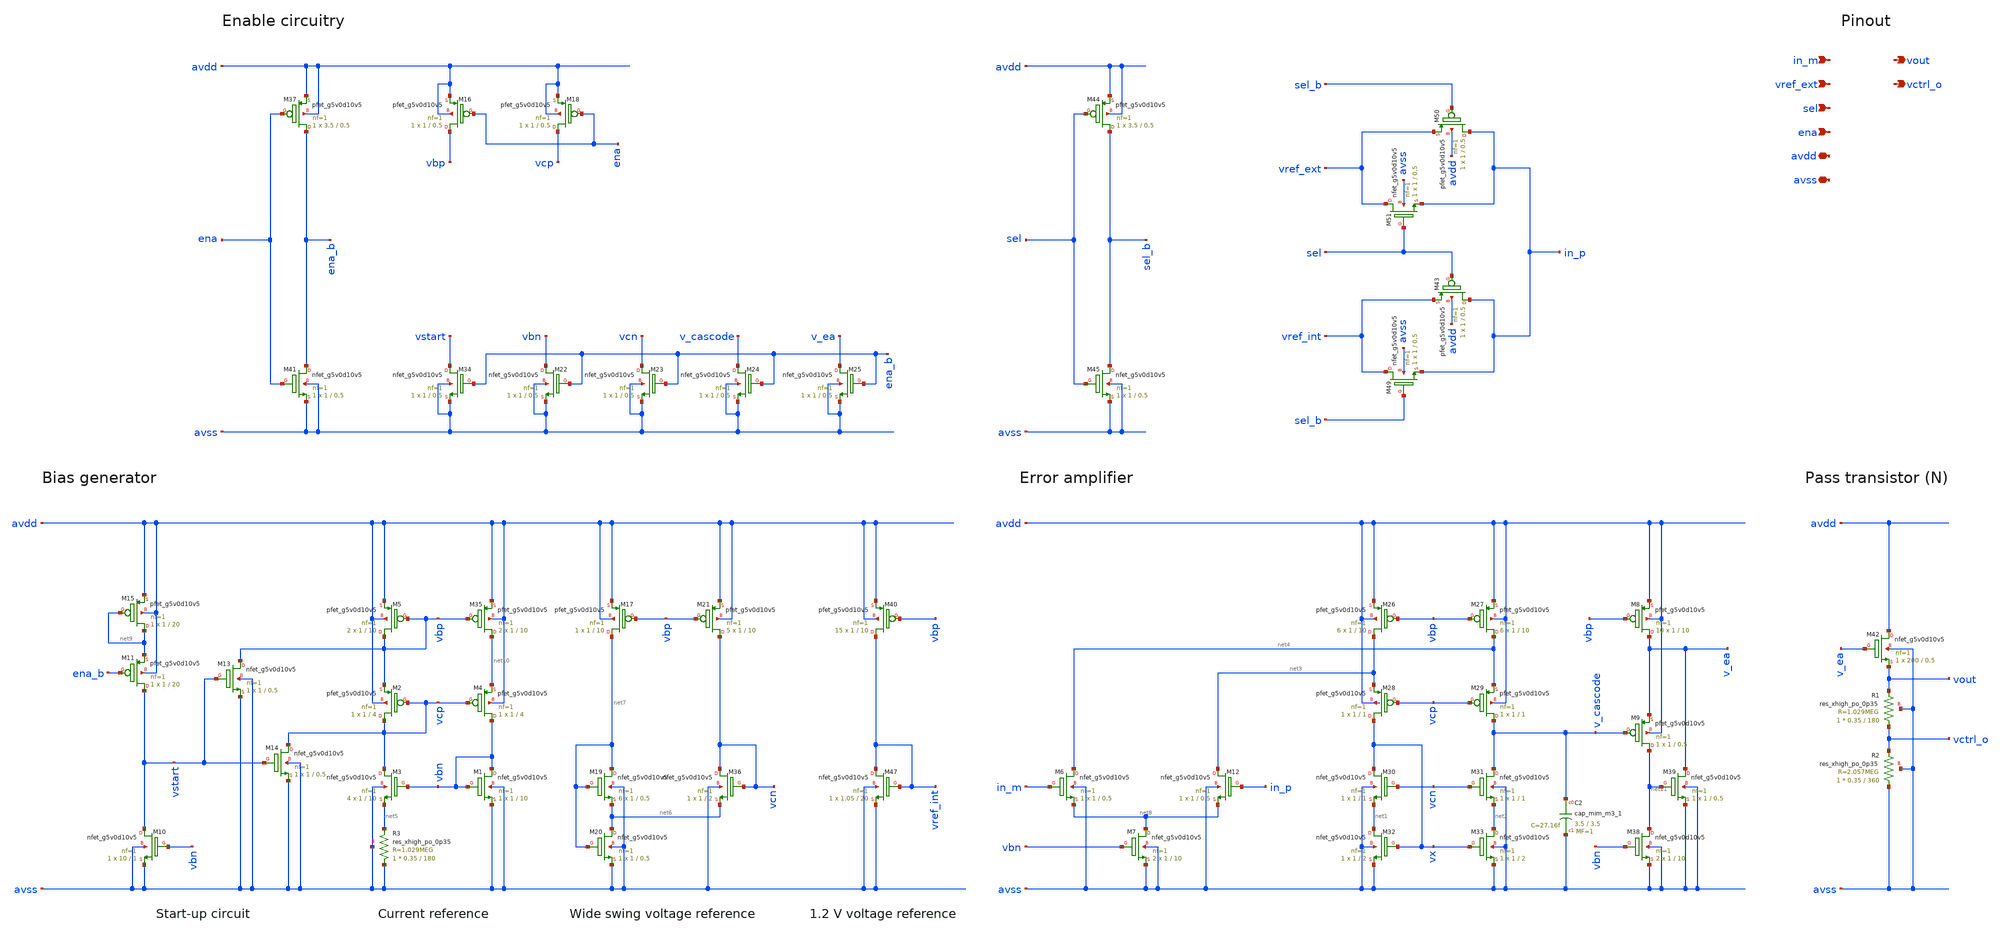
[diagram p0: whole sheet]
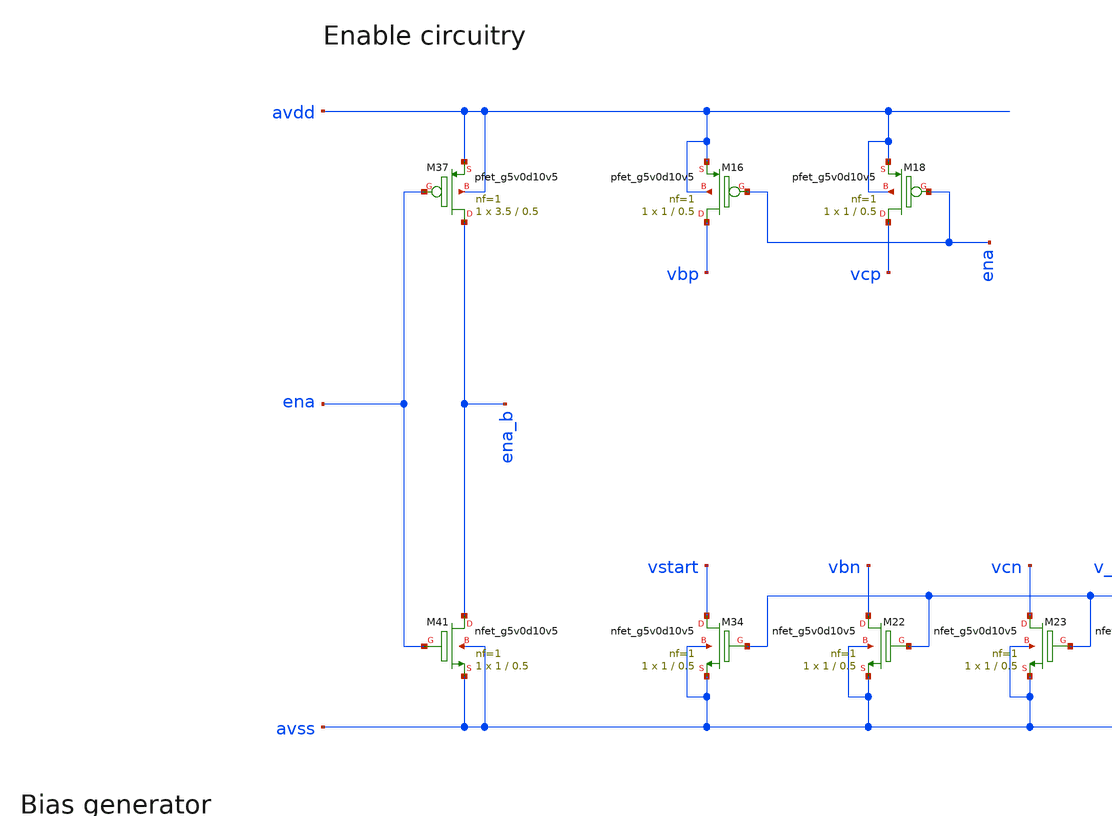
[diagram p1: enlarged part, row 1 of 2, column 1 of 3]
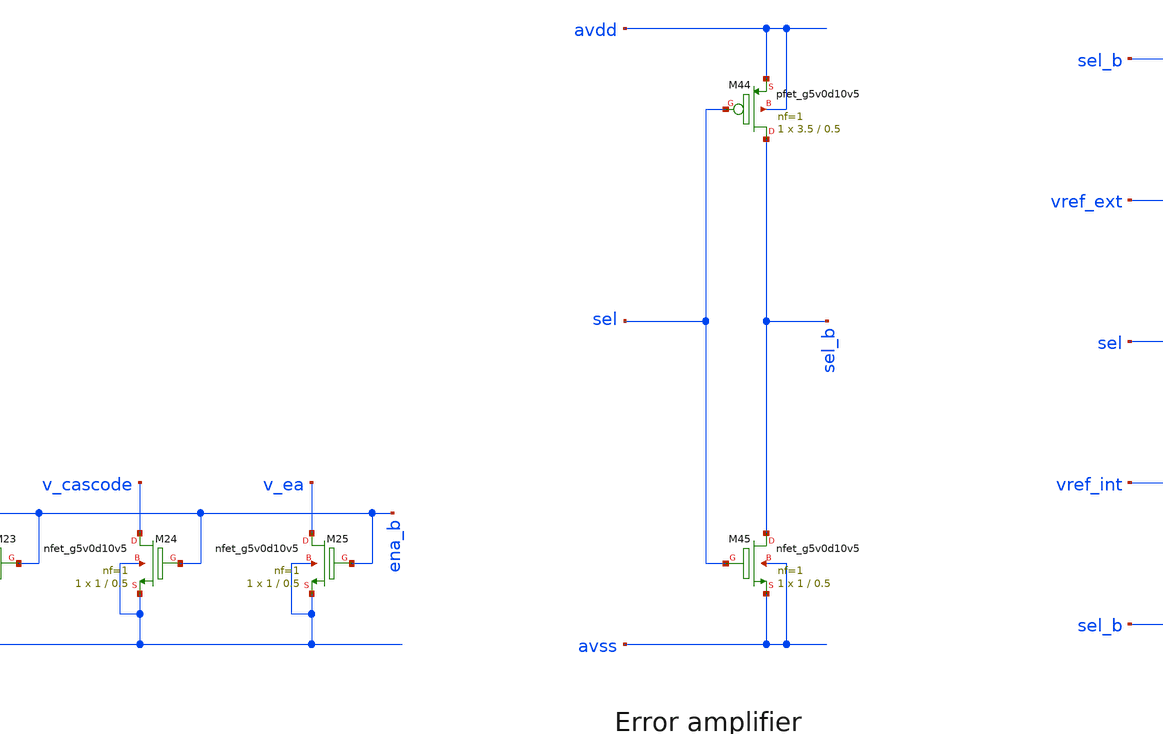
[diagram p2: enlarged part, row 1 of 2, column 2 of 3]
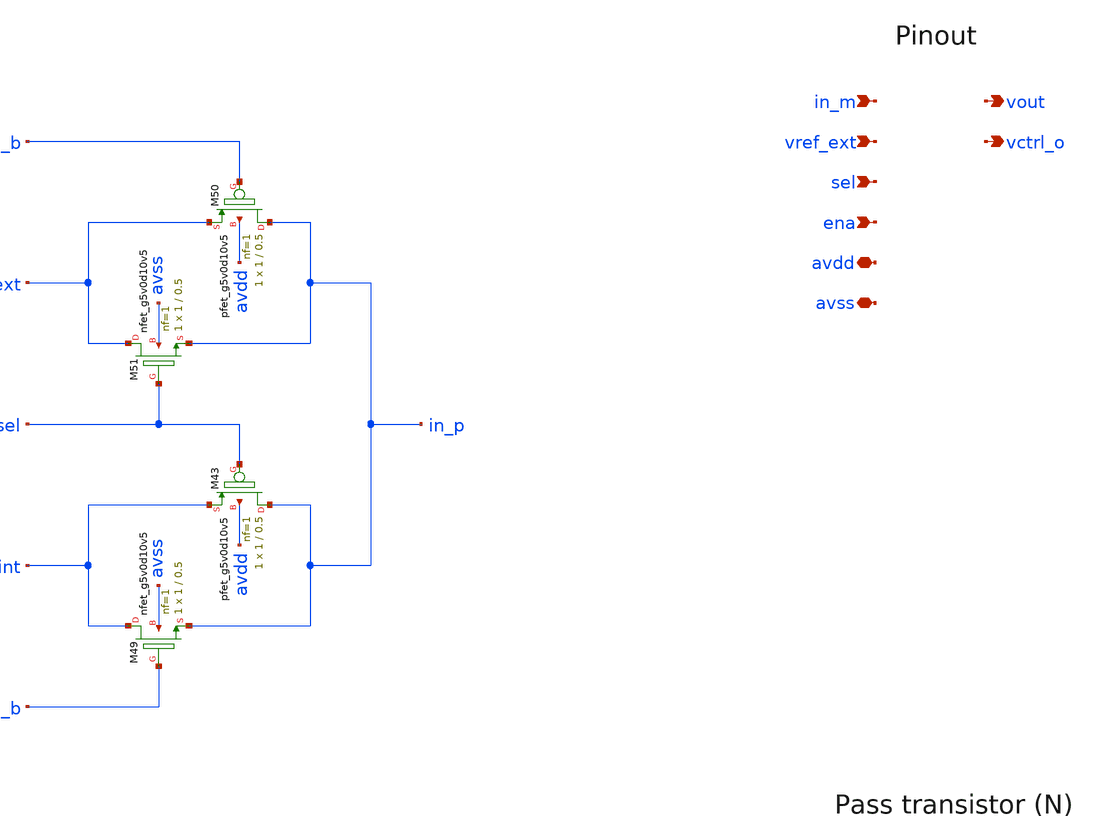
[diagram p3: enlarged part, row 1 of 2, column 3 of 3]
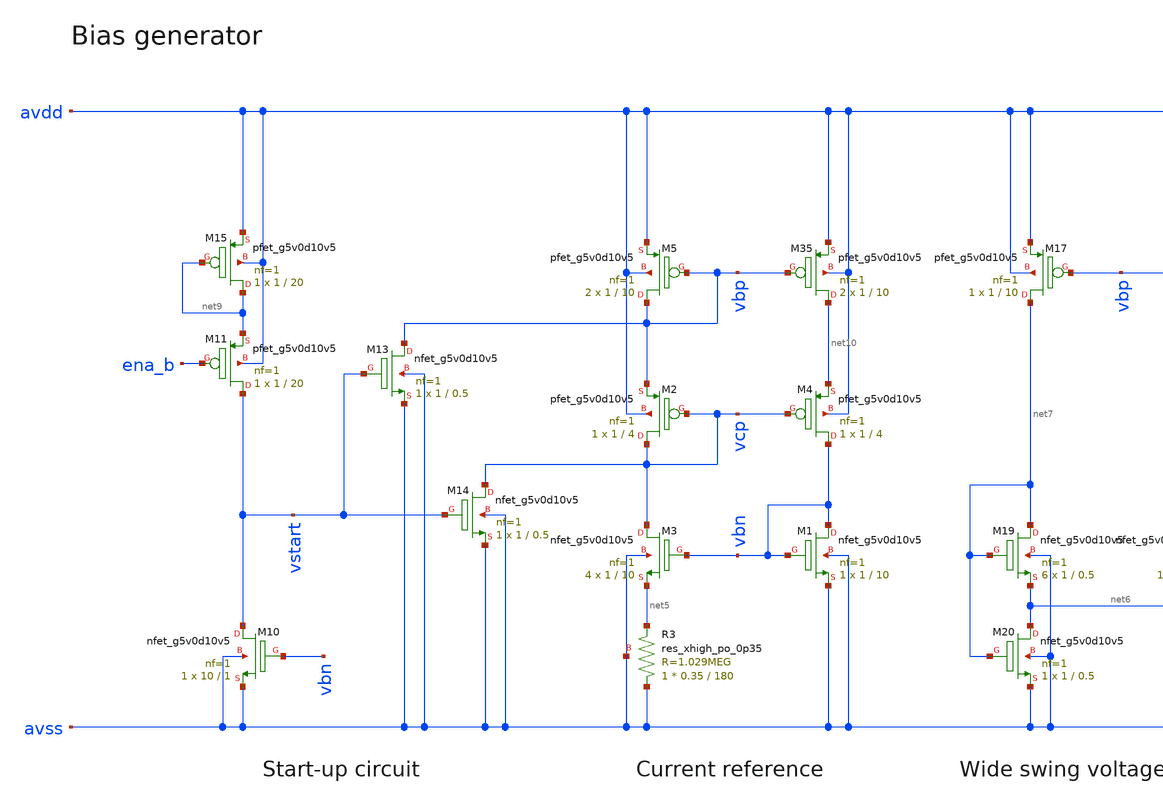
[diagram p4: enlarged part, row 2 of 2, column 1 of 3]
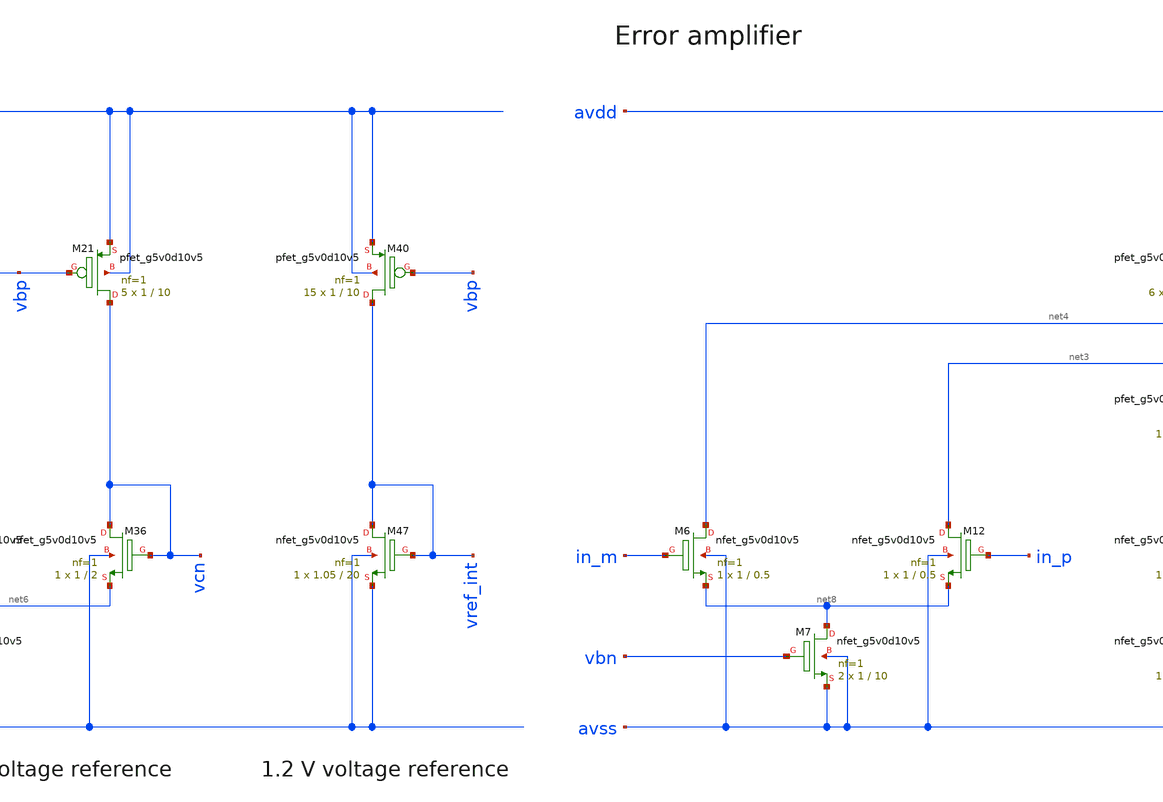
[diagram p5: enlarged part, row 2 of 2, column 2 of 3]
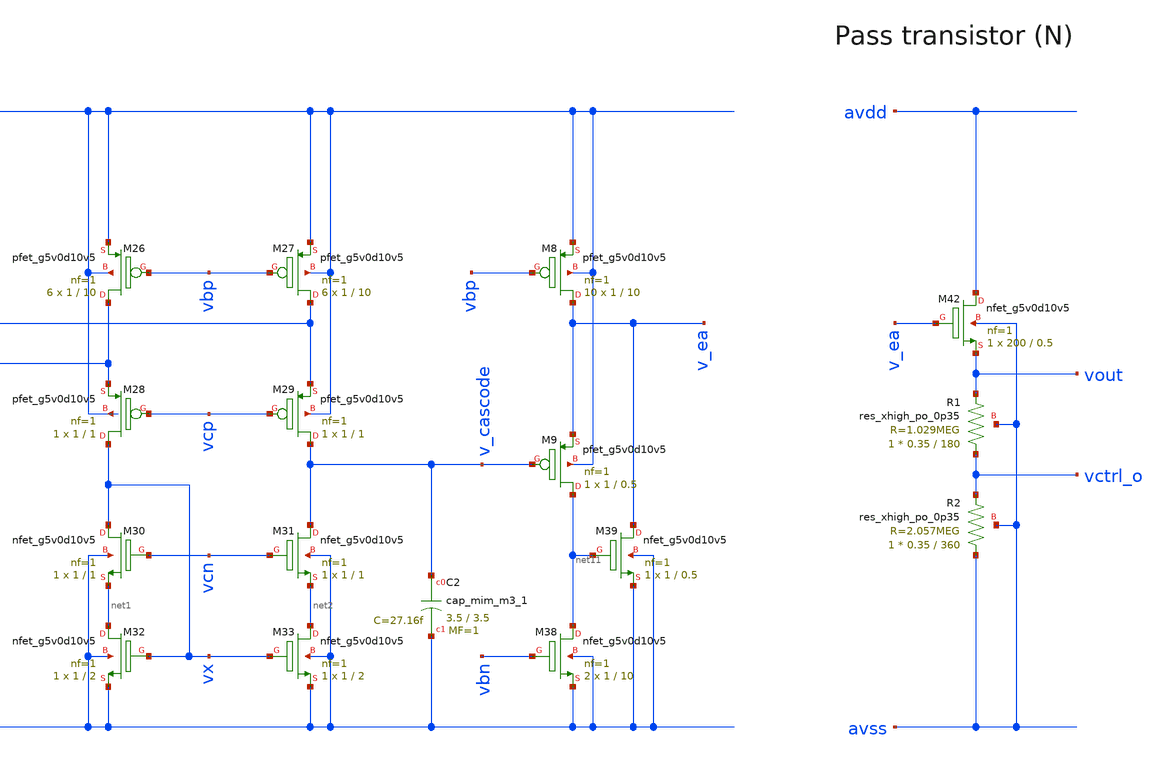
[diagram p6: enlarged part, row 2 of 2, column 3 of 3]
** sch_path: xschem/error_amplifier_03v3.sch
**.subckt error_amplifier_03v3 in_m ena avdd avss vout vctrl_o sel vref_ext
*.ipin in_m
*.ipin ena
*.iopin avdd
*.iopin avss
*.opin vout
*.opin vctrl_o
*.ipin sel
*.ipin vref_ext
XM1 vbn vbn avss avss sky130_fd_pr__nfet_g5v0d10v5 L=10 W=1 nf=1 ad='int((nf+1)/2) * W/nf * 0.29' as='int((nf+2)/2) * W/nf * 0.29'
+ pd='2*int((nf+1)/2) * (W/nf + 0.29)' ps='2*int((nf+2)/2) * (W/nf + 0.29)' nrd='0.29 / W' nrs='0.29 / W'
+ sa=0 sb=0 sd=0 mult=1 m=1
XM3 vcp vbn net5 avss sky130_fd_pr__nfet_g5v0d10v5 L=10 W=1 nf=1 ad='int((nf+1)/2) * W/nf * 0.29' as='int((nf+2)/2) * W/nf * 0.29'
+ pd='2*int((nf+1)/2) * (W/nf + 0.29)' ps='2*int((nf+2)/2) * (W/nf + 0.29)' nrd='0.29 / W' nrs='0.29 / W'
+ sa=0 sb=0 sd=0 mult=4 m=4
XM5 vbp vbp avdd avdd sky130_fd_pr__pfet_g5v0d10v5 L=10 W=1 nf=1 ad='int((nf+1)/2) * W/nf * 0.29' as='int((nf+2)/2) * W/nf * 0.29'
+ pd='2*int((nf+1)/2) * (W/nf + 0.29)' ps='2*int((nf+2)/2) * (W/nf + 0.29)' nrd='0.29 / W' nrs='0.29 / W'
+ sa=0 sb=0 sd=0 mult=2 m=2
XM26 net3 vbp avdd avdd sky130_fd_pr__pfet_g5v0d10v5 L=10 W=1 nf=1 ad='int((nf+1)/2) * W/nf * 0.29' as='int((nf+2)/2) * W/nf * 0.29'
+ pd='2*int((nf+1)/2) * (W/nf + 0.29)' ps='2*int((nf+2)/2) * (W/nf + 0.29)' nrd='0.29 / W' nrs='0.29 / W'
+ sa=0 sb=0 sd=0 mult=6 m=6
XM27 net4 vbp avdd avdd sky130_fd_pr__pfet_g5v0d10v5 L=10 W=1 nf=1 ad='int((nf+1)/2) * W/nf * 0.29' as='int((nf+2)/2) * W/nf * 0.29'
+ pd='2*int((nf+1)/2) * (W/nf + 0.29)' ps='2*int((nf+2)/2) * (W/nf + 0.29)' nrd='0.29 / W' nrs='0.29 / W'
+ sa=0 sb=0 sd=0 mult=6 m=6
XM28 vx vcp net3 avdd sky130_fd_pr__pfet_g5v0d10v5 L=1 W=1 nf=1 ad='int((nf+1)/2) * W/nf * 0.29' as='int((nf+2)/2) * W/nf * 0.29'
+ pd='2*int((nf+1)/2) * (W/nf + 0.29)' ps='2*int((nf+2)/2) * (W/nf + 0.29)' nrd='0.29 / W' nrs='0.29 / W'
+ sa=0 sb=0 sd=0 mult=1 m=1
XM29 v_cascode vcp net4 avdd sky130_fd_pr__pfet_g5v0d10v5 L=1 W=1 nf=1 ad='int((nf+1)/2) * W/nf * 0.29'
+ as='int((nf+2)/2) * W/nf * 0.29' pd='2*int((nf+1)/2) * (W/nf + 0.29)' ps='2*int((nf+2)/2) * (W/nf + 0.29)'
+ nrd='0.29 / W' nrs='0.29 / W' sa=0 sb=0 sd=0 mult=1 m=1
XM30 vx vcn net1 avss sky130_fd_pr__nfet_g5v0d10v5 L=1 W=1 nf=1 ad='int((nf+1)/2) * W/nf * 0.29' as='int((nf+2)/2) * W/nf * 0.29'
+ pd='2*int((nf+1)/2) * (W/nf + 0.29)' ps='2*int((nf+2)/2) * (W/nf + 0.29)' nrd='0.29 / W' nrs='0.29 / W'
+ sa=0 sb=0 sd=0 mult=1 m=1
XM31 v_cascode vcn net2 avss sky130_fd_pr__nfet_g5v0d10v5 L=1 W=1 nf=1 ad='int((nf+1)/2) * W/nf * 0.29'
+ as='int((nf+2)/2) * W/nf * 0.29' pd='2*int((nf+1)/2) * (W/nf + 0.29)' ps='2*int((nf+2)/2) * (W/nf + 0.29)'
+ nrd='0.29 / W' nrs='0.29 / W' sa=0 sb=0 sd=0 mult=1 m=1
XM32 net1 vx avss avss sky130_fd_pr__nfet_g5v0d10v5 L=2 W=1 nf=1 ad='int((nf+1)/2) * W/nf * 0.29' as='int((nf+2)/2) * W/nf * 0.29'
+ pd='2*int((nf+1)/2) * (W/nf + 0.29)' ps='2*int((nf+2)/2) * (W/nf + 0.29)' nrd='0.29 / W' nrs='0.29 / W'
+ sa=0 sb=0 sd=0 mult=1 m=1
XM33 net2 vx avss avss sky130_fd_pr__nfet_g5v0d10v5 L=2 W=1 nf=1 ad='int((nf+1)/2) * W/nf * 0.29' as='int((nf+2)/2) * W/nf * 0.29'
+ pd='2*int((nf+1)/2) * (W/nf + 0.29)' ps='2*int((nf+2)/2) * (W/nf + 0.29)' nrd='0.29 / W' nrs='0.29 / W'
+ sa=0 sb=0 sd=0 mult=1 m=1
XM35 net10 vbp avdd avdd sky130_fd_pr__pfet_g5v0d10v5 L=10 W=1 nf=1 ad='int((nf+1)/2) * W/nf * 0.29'
+ as='int((nf+2)/2) * W/nf * 0.29' pd='2*int((nf+1)/2) * (W/nf + 0.29)' ps='2*int((nf+2)/2) * (W/nf + 0.29)'
+ nrd='0.29 / W' nrs='0.29 / W' sa=0 sb=0 sd=0 mult=2 m=2
XR3 avss net5 avss sky130_fd_pr__res_xhigh_po_0p35 L=180 mult=1 m=1
XM9 net11 v_cascode v_ea avdd sky130_fd_pr__pfet_g5v0d10v5 L=0.5 W=1 nf=1 ad='int((nf+1)/2) * W/nf * 0.29'
+ as='int((nf+2)/2) * W/nf * 0.29' pd='2*int((nf+1)/2) * (W/nf + 0.29)' ps='2*int((nf+2)/2) * (W/nf + 0.29)'
+ nrd='0.29 / W' nrs='0.29 / W' sa=0 sb=0 sd=0 mult=1 m=1
XM8 v_ea vbp avdd avdd sky130_fd_pr__pfet_g5v0d10v5 L=10 W=1 nf=1 ad='int((nf+1)/2) * W/nf * 0.29' as='int((nf+2)/2) * W/nf * 0.29'
+ pd='2*int((nf+1)/2) * (W/nf + 0.29)' ps='2*int((nf+2)/2) * (W/nf + 0.29)' nrd='0.29 / W' nrs='0.29 / W'
+ sa=0 sb=0 sd=0 mult=10 m=10
XM17 net7 vbp avdd avdd sky130_fd_pr__pfet_g5v0d10v5 L=10 W=1 nf=1 ad='int((nf+1)/2) * W/nf * 0.29' as='int((nf+2)/2) * W/nf * 0.29'
+ pd='2*int((nf+1)/2) * (W/nf + 0.29)' ps='2*int((nf+2)/2) * (W/nf + 0.29)' nrd='0.29 / W' nrs='0.29 / W'
+ sa=0 sb=0 sd=0 mult=1 m=1
XM19 net7 net7 net6 avss sky130_fd_pr__nfet_g5v0d10v5 L=0.5 W=1 nf=1 ad='int((nf+1)/2) * W/nf * 0.29'
+ as='int((nf+2)/2) * W/nf * 0.29' pd='2*int((nf+1)/2) * (W/nf + 0.29)' ps='2*int((nf+2)/2) * (W/nf + 0.29)'
+ nrd='0.29 / W' nrs='0.29 / W' sa=0 sb=0 sd=0 mult=6 m=6
XM20 net6 net7 avss avss sky130_fd_pr__nfet_g5v0d10v5 L=0.5 W=1 nf=1 ad='int((nf+1)/2) * W/nf * 0.29'
+ as='int((nf+2)/2) * W/nf * 0.29' pd='2*int((nf+1)/2) * (W/nf + 0.29)' ps='2*int((nf+2)/2) * (W/nf + 0.29)'
+ nrd='0.29 / W' nrs='0.29 / W' sa=0 sb=0 sd=0 mult=1 m=1
XM21 vcn vbp avdd avdd sky130_fd_pr__pfet_g5v0d10v5 L=10 W=1 nf=1 ad='int((nf+1)/2) * W/nf * 0.29' as='int((nf+2)/2) * W/nf * 0.29'
+ pd='2*int((nf+1)/2) * (W/nf + 0.29)' ps='2*int((nf+2)/2) * (W/nf + 0.29)' nrd='0.29 / W' nrs='0.29 / W'
+ sa=0 sb=0 sd=0 mult=5 m=5
XM36 vcn vcn net6 avss sky130_fd_pr__nfet_g5v0d10v5 L=2 W=1 nf=1 ad='int((nf+1)/2) * W/nf * 0.29' as='int((nf+2)/2) * W/nf * 0.29'
+ pd='2*int((nf+1)/2) * (W/nf + 0.29)' ps='2*int((nf+2)/2) * (W/nf + 0.29)' nrd='0.29 / W' nrs='0.29 / W'
+ sa=0 sb=0 sd=0 mult=1 m=1
XM6 net4 in_m net8 avss sky130_fd_pr__nfet_g5v0d10v5 L=0.5 W=1 nf=1 ad='int((nf+1)/2) * W/nf * 0.29'
+ as='int((nf+2)/2) * W/nf * 0.29' pd='2*int((nf+1)/2) * (W/nf + 0.29)' ps='2*int((nf+2)/2) * (W/nf + 0.29)'
+ nrd='0.29 / W' nrs='0.29 / W' sa=0 sb=0 sd=0 mult=1 m=1
XM7 net8 vbn avss avss sky130_fd_pr__nfet_g5v0d10v5 L=10 W=1 nf=1 ad='int((nf+1)/2) * W/nf * 0.29' as='int((nf+2)/2) * W/nf * 0.29'
+ pd='2*int((nf+1)/2) * (W/nf + 0.29)' ps='2*int((nf+2)/2) * (W/nf + 0.29)' nrd='0.29 / W' nrs='0.29 / W'
+ sa=0 sb=0 sd=0 mult=2 m=2
XM12 net3 in_p net8 avss sky130_fd_pr__nfet_g5v0d10v5 L=0.5 W=1 nf=1 ad='int((nf+1)/2) * W/nf * 0.29'
+ as='int((nf+2)/2) * W/nf * 0.29' pd='2*int((nf+1)/2) * (W/nf + 0.29)' ps='2*int((nf+2)/2) * (W/nf + 0.29)'
+ nrd='0.29 / W' nrs='0.29 / W' sa=0 sb=0 sd=0 mult=1 m=1
XM10 vstart vbn avss avss sky130_fd_pr__nfet_g5v0d10v5 L=1 W=10 nf=1 ad='int((nf+1)/2) * W/nf * 0.29'
+ as='int((nf+2)/2) * W/nf * 0.29' pd='2*int((nf+1)/2) * (W/nf + 0.29)' ps='2*int((nf+2)/2) * (W/nf + 0.29)'
+ nrd='0.29 / W' nrs='0.29 / W' sa=0 sb=0 sd=0 mult=1 m=1
XM11 vstart ena_b net9 avdd sky130_fd_pr__pfet_g5v0d10v5 L=20 W=1 nf=1 ad='int((nf+1)/2) * W/nf * 0.29'
+ as='int((nf+2)/2) * W/nf * 0.29' pd='2*int((nf+1)/2) * (W/nf + 0.29)' ps='2*int((nf+2)/2) * (W/nf + 0.29)'
+ nrd='0.29 / W' nrs='0.29 / W' sa=0 sb=0 sd=0 mult=1 m=1
XM2 vcp vcp vbp avdd sky130_fd_pr__pfet_g5v0d10v5 L=4 W=1 nf=1 ad='int((nf+1)/2) * W/nf * 0.29' as='int((nf+2)/2) * W/nf * 0.29'
+ pd='2*int((nf+1)/2) * (W/nf + 0.29)' ps='2*int((nf+2)/2) * (W/nf + 0.29)' nrd='0.29 / W' nrs='0.29 / W'
+ sa=0 sb=0 sd=0 mult=1 m=1
XM4 vbn vcp net10 avdd sky130_fd_pr__pfet_g5v0d10v5 L=4 W=1 nf=1 ad='int((nf+1)/2) * W/nf * 0.29' as='int((nf+2)/2) * W/nf * 0.29'
+ pd='2*int((nf+1)/2) * (W/nf + 0.29)' ps='2*int((nf+2)/2) * (W/nf + 0.29)' nrd='0.29 / W' nrs='0.29 / W'
+ sa=0 sb=0 sd=0 mult=1 m=1
XM13 vbp vstart avss avss sky130_fd_pr__nfet_g5v0d10v5 L=0.5 W=1 nf=1 ad='int((nf+1)/2) * W/nf * 0.29'
+ as='int((nf+2)/2) * W/nf * 0.29' pd='2*int((nf+1)/2) * (W/nf + 0.29)' ps='2*int((nf+2)/2) * (W/nf + 0.29)'
+ nrd='0.29 / W' nrs='0.29 / W' sa=0 sb=0 sd=0 mult=1 m=1
XM14 vcp vstart avss avss sky130_fd_pr__nfet_g5v0d10v5 L=0.5 W=1 nf=1 ad='int((nf+1)/2) * W/nf * 0.29'
+ as='int((nf+2)/2) * W/nf * 0.29' pd='2*int((nf+1)/2) * (W/nf + 0.29)' ps='2*int((nf+2)/2) * (W/nf + 0.29)'
+ nrd='0.29 / W' nrs='0.29 / W' sa=0 sb=0 sd=0 mult=1 m=1
XM15 net9 net9 avdd avdd sky130_fd_pr__pfet_g5v0d10v5 L=20 W=1 nf=1 ad='int((nf+1)/2) * W/nf * 0.29'
+ as='int((nf+2)/2) * W/nf * 0.29' pd='2*int((nf+1)/2) * (W/nf + 0.29)' ps='2*int((nf+2)/2) * (W/nf + 0.29)'
+ nrd='0.29 / W' nrs='0.29 / W' sa=0 sb=0 sd=0 mult=1 m=1
XM16 vbp ena avdd avdd sky130_fd_pr__pfet_g5v0d10v5 L=0.5 W=1 nf=1 ad='int((nf+1)/2) * W/nf * 0.29' as='int((nf+2)/2) * W/nf * 0.29'
+ pd='2*int((nf+1)/2) * (W/nf + 0.29)' ps='2*int((nf+2)/2) * (W/nf + 0.29)' nrd='0.29 / W' nrs='0.29 / W'
+ sa=0 sb=0 sd=0 mult=1 m=1
XM18 vcp ena avdd avdd sky130_fd_pr__pfet_g5v0d10v5 L=0.5 W=1 nf=1 ad='int((nf+1)/2) * W/nf * 0.29' as='int((nf+2)/2) * W/nf * 0.29'
+ pd='2*int((nf+1)/2) * (W/nf + 0.29)' ps='2*int((nf+2)/2) * (W/nf + 0.29)' nrd='0.29 / W' nrs='0.29 / W'
+ sa=0 sb=0 sd=0 mult=1 m=1
XM22 vbn ena_b avss avss sky130_fd_pr__nfet_g5v0d10v5 L=0.5 W=1 nf=1 ad='int((nf+1)/2) * W/nf * 0.29'
+ as='int((nf+2)/2) * W/nf * 0.29' pd='2*int((nf+1)/2) * (W/nf + 0.29)' ps='2*int((nf+2)/2) * (W/nf + 0.29)'
+ nrd='0.29 / W' nrs='0.29 / W' sa=0 sb=0 sd=0 mult=1 m=1
XM23 vcn ena_b avss avss sky130_fd_pr__nfet_g5v0d10v5 L=0.5 W=1 nf=1 ad='int((nf+1)/2) * W/nf * 0.29'
+ as='int((nf+2)/2) * W/nf * 0.29' pd='2*int((nf+1)/2) * (W/nf + 0.29)' ps='2*int((nf+2)/2) * (W/nf + 0.29)'
+ nrd='0.29 / W' nrs='0.29 / W' sa=0 sb=0 sd=0 mult=1 m=1
XM24 v_cascode ena_b avss avss sky130_fd_pr__nfet_g5v0d10v5 L=0.5 W=1 nf=1 ad='int((nf+1)/2) * W/nf * 0.29'
+ as='int((nf+2)/2) * W/nf * 0.29' pd='2*int((nf+1)/2) * (W/nf + 0.29)' ps='2*int((nf+2)/2) * (W/nf + 0.29)'
+ nrd='0.29 / W' nrs='0.29 / W' sa=0 sb=0 sd=0 mult=1 m=1
XM25 v_ea ena_b avss avss sky130_fd_pr__nfet_g5v0d10v5 L=0.5 W=1 nf=1 ad='int((nf+1)/2) * W/nf * 0.29'
+ as='int((nf+2)/2) * W/nf * 0.29' pd='2*int((nf+1)/2) * (W/nf + 0.29)' ps='2*int((nf+2)/2) * (W/nf + 0.29)'
+ nrd='0.29 / W' nrs='0.29 / W' sa=0 sb=0 sd=0 mult=1 m=1
XM34 vstart ena_b avss avss sky130_fd_pr__nfet_g5v0d10v5 L=0.5 W=1 nf=1 ad='int((nf+1)/2) * W/nf * 0.29'
+ as='int((nf+2)/2) * W/nf * 0.29' pd='2*int((nf+1)/2) * (W/nf + 0.29)' ps='2*int((nf+2)/2) * (W/nf + 0.29)'
+ nrd='0.29 / W' nrs='0.29 / W' sa=0 sb=0 sd=0 mult=1 m=1
XM38 net11 vbn avss avss sky130_fd_pr__nfet_g5v0d10v5 L=10 W=1 nf=1 ad='int((nf+1)/2) * W/nf * 0.29'
+ as='int((nf+2)/2) * W/nf * 0.29' pd='2*int((nf+1)/2) * (W/nf + 0.29)' ps='2*int((nf+2)/2) * (W/nf + 0.29)'
+ nrd='0.29 / W' nrs='0.29 / W' sa=0 sb=0 sd=0 mult=2 m=2
XM39 v_ea net11 avss avss sky130_fd_pr__nfet_g5v0d10v5 L=0.5 W=1 nf=1 ad='int((nf+1)/2) * W/nf * 0.29'
+ as='int((nf+2)/2) * W/nf * 0.29' pd='2*int((nf+1)/2) * (W/nf + 0.29)' ps='2*int((nf+2)/2) * (W/nf + 0.29)'
+ nrd='0.29 / W' nrs='0.29 / W' sa=0 sb=0 sd=0 mult=1 m=1
XM40 vref_int vbp avdd avdd sky130_fd_pr__pfet_g5v0d10v5 L=10 W=1 nf=1 ad='int((nf+1)/2) * W/nf * 0.29'
+ as='int((nf+2)/2) * W/nf * 0.29' pd='2*int((nf+1)/2) * (W/nf + 0.29)' ps='2*int((nf+2)/2) * (W/nf + 0.29)'
+ nrd='0.29 / W' nrs='0.29 / W' sa=0 sb=0 sd=0 mult=15 m=15
XM47 vref_int vref_int avss avss sky130_fd_pr__nfet_g5v0d10v5 L=20 W=1.05 nf=1 ad='int((nf+1)/2) * W/nf * 0.29'
+ as='int((nf+2)/2) * W/nf * 0.29' pd='2*int((nf+1)/2) * (W/nf + 0.29)' ps='2*int((nf+2)/2) * (W/nf + 0.29)'
+ nrd='0.29 / W' nrs='0.29 / W' sa=0 sb=0 sd=0 mult=1 m=1
XM37 ena_b ena avdd avdd sky130_fd_pr__pfet_g5v0d10v5 L=0.5 W=3.5 nf=1 ad='int((nf+1)/2) * W/nf * 0.29'
+ as='int((nf+2)/2) * W/nf * 0.29' pd='2*int((nf+1)/2) * (W/nf + 0.29)' ps='2*int((nf+2)/2) * (W/nf + 0.29)'
+ nrd='0.29 / W' nrs='0.29 / W' sa=0 sb=0 sd=0 mult=1 m=1
XM41 ena_b ena avss avss sky130_fd_pr__nfet_g5v0d10v5 L=0.5 W=1 nf=1 ad='int((nf+1)/2) * W/nf * 0.29'
+ as='int((nf+2)/2) * W/nf * 0.29' pd='2*int((nf+1)/2) * (W/nf + 0.29)' ps='2*int((nf+2)/2) * (W/nf + 0.29)'
+ nrd='0.29 / W' nrs='0.29 / W' sa=0 sb=0 sd=0 mult=1 m=1
XC2 v_cascode avss sky130_fd_pr__cap_mim_m3_1 W=3.5 L=3.5 MF=1 m=1
XR1 vctrl_o vout avss sky130_fd_pr__res_xhigh_po_0p35 L=180 mult=1 m=1
XR2 avss vctrl_o avss sky130_fd_pr__res_xhigh_po_0p35 L=360 mult=1 m=1
XM42 avdd v_ea vout avss sky130_fd_pr__nfet_g5v0d10v5 L=0.5 W=200 nf=1 ad='int((nf+1)/2) * W/nf * 0.29'
+ as='int((nf+2)/2) * W/nf * 0.29' pd='2*int((nf+1)/2) * (W/nf + 0.29)' ps='2*int((nf+2)/2) * (W/nf + 0.29)'
+ nrd='0.29 / W' nrs='0.29 / W' sa=0 sb=0 sd=0 mult=1 m=1
XM43 in_p sel vref_int avdd sky130_fd_pr__pfet_g5v0d10v5 L=0.5 W=1 nf=1 ad='int((nf+1)/2) * W/nf * 0.29'
+ as='int((nf+2)/2) * W/nf * 0.29' pd='2*int((nf+1)/2) * (W/nf + 0.29)' ps='2*int((nf+2)/2) * (W/nf + 0.29)'
+ nrd='0.29 / W' nrs='0.29 / W' sa=0 sb=0 sd=0 mult=1 m=1
XM49 vref_int sel_b in_p avss sky130_fd_pr__nfet_g5v0d10v5 L=0.5 W=1 nf=1 ad='int((nf+1)/2) * W/nf * 0.29'
+ as='int((nf+2)/2) * W/nf * 0.29' pd='2*int((nf+1)/2) * (W/nf + 0.29)' ps='2*int((nf+2)/2) * (W/nf + 0.29)'
+ nrd='0.29 / W' nrs='0.29 / W' sa=0 sb=0 sd=0 mult=1 m=1
XM50 in_p sel_b vref_ext avdd sky130_fd_pr__pfet_g5v0d10v5 L=0.5 W=1 nf=1 ad='int((nf+1)/2) * W/nf * 0.29'
+ as='int((nf+2)/2) * W/nf * 0.29' pd='2*int((nf+1)/2) * (W/nf + 0.29)' ps='2*int((nf+2)/2) * (W/nf + 0.29)'
+ nrd='0.29 / W' nrs='0.29 / W' sa=0 sb=0 sd=0 mult=1 m=1
XM51 vref_ext sel in_p avss sky130_fd_pr__nfet_g5v0d10v5 L=0.5 W=1 nf=1 ad='int((nf+1)/2) * W/nf * 0.29'
+ as='int((nf+2)/2) * W/nf * 0.29' pd='2*int((nf+1)/2) * (W/nf + 0.29)' ps='2*int((nf+2)/2) * (W/nf + 0.29)'
+ nrd='0.29 / W' nrs='0.29 / W' sa=0 sb=0 sd=0 mult=1 m=1
XM44 sel_b sel avdd avdd sky130_fd_pr__pfet_g5v0d10v5 L=0.5 W=3.5 nf=1 ad='int((nf+1)/2) * W/nf * 0.29'
+ as='int((nf+2)/2) * W/nf * 0.29' pd='2*int((nf+1)/2) * (W/nf + 0.29)' ps='2*int((nf+2)/2) * (W/nf + 0.29)'
+ nrd='0.29 / W' nrs='0.29 / W' sa=0 sb=0 sd=0 mult=1 m=1
XM45 sel_b sel avss avss sky130_fd_pr__nfet_g5v0d10v5 L=0.5 W=1 nf=1 ad='int((nf+1)/2) * W/nf * 0.29'
+ as='int((nf+2)/2) * W/nf * 0.29' pd='2*int((nf+1)/2) * (W/nf + 0.29)' ps='2*int((nf+2)/2) * (W/nf + 0.29)'
+ nrd='0.29 / W' nrs='0.29 / W' sa=0 sb=0 sd=0 mult=1 m=1
**.ends
.end
